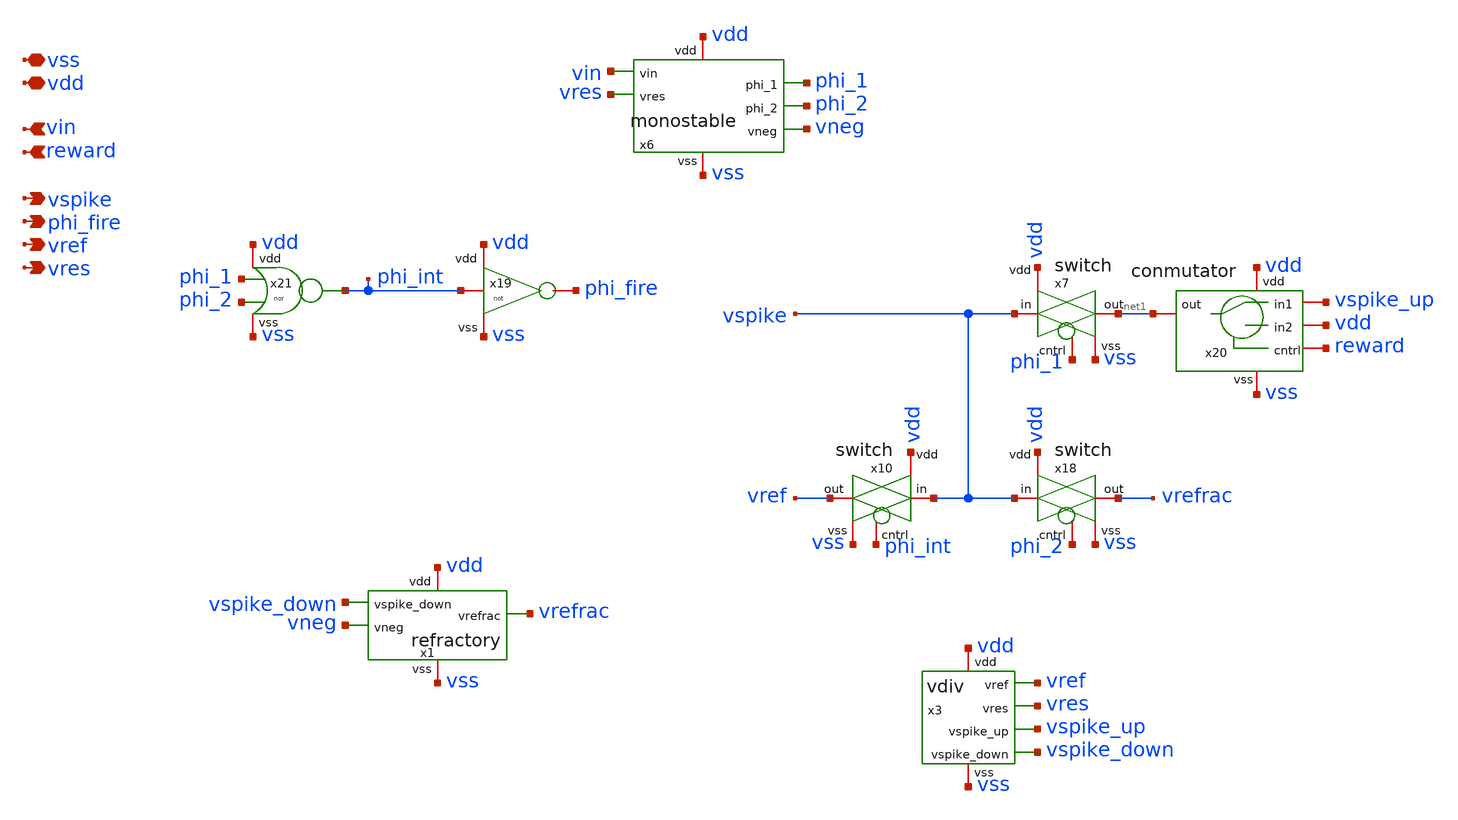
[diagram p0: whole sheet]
** sch_path: designs/libs/core_LIF_comp/core_phaseUpulse/phaseUpulse.sch
**.subckt phaseUpulse vin vdd vss vspike phi_fire vref reward vres
*.ipin vin
*.iopin vdd
*.iopin vss
*.opin vspike
*.opin phi_fire
*.opin vref
*.ipin reward
*.opin vres
x19 vdd phi_int phi_fire vss not
x21 vdd vss phi_1 phi_2 phi_int nor
x7 vdd vspike net1 phi_1 vss switch
x10 vdd vspike vref phi_int vss switch
x18 vdd vspike vrefrac phi_2 vss switch
x20 reward vdd vdd net1 vspike_up vss conmutator
x6 vss vdd vin vres phi_1 phi_2 vneg monostable
x1 vss vdd vspike_down vneg vrefrac refractory
x3 vss vdd vref vspike_up vspike_down vres vdiv
**.ends
.end
